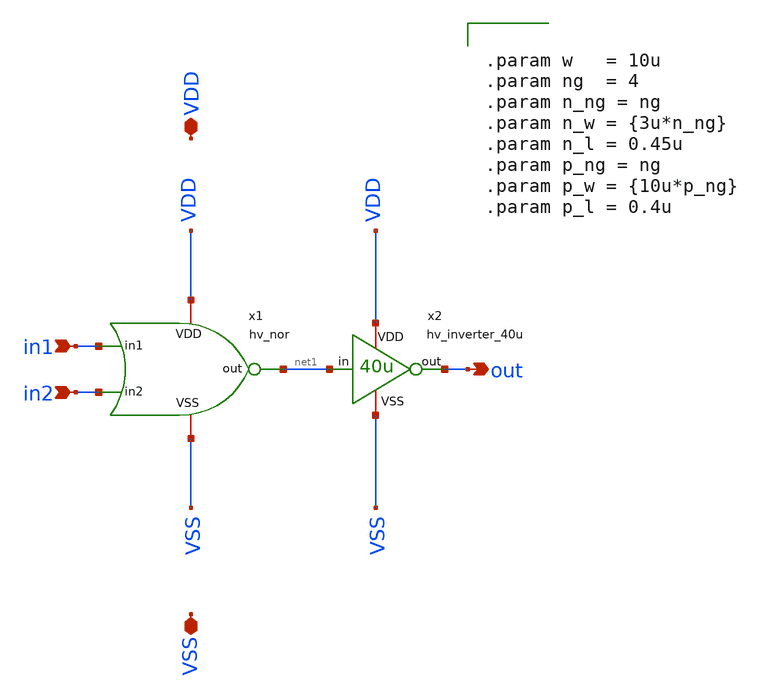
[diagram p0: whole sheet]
** sch_path: macros/heichips26_vcr/macros/switched_capacitor/schematic/xschem/hv_or.sch
**.subckt hv_or in1 VDD VSS in2 out
*.ipin in1
*.iopin VDD
*.iopin VSS
*.ipin in2
*.opin out
x1 VDD in1 net1 in2 VSS hv_nor
x2 VDD net1 out VSS hv_inverter_40u
**** begin user architecture code


.param w   = 10u
.param ng  = 4
.param n_ng = ng
.param n_w = {3u*n_ng}
.param n_l = 0.45u
.param p_ng = ng
.param p_w = {10u*p_ng}
.param p_l = 0.4u


**** end user architecture code
**.ends

* expanding   symbol:  hv_nor.sym # of pins=5
** sym_path: macros/heichips26_vcr/macros/switched_capacitor/schematic/xschem/hv_nor.sym
** sch_path: macros/heichips26_vcr/macros/switched_capacitor/schematic/xschem/hv_nor.sch
.subckt hv_nor VDD in1 out in2 VSS
*.ipin in1
*.iopin VDD
*.iopin VSS
*.opin out
*.ipin in2
**** begin user architecture code


.param w   = 10u
.param ng  = 4
.param n_ng = ng
.param n_w = {3u*n_ng}
.param n_l = 0.45u
.param p_ng = ng
.param p_w = {10u*p_ng}
.param p_l = 0.4u


**** end user architecture code
XM2 out in2 VSS VSS sg13_hv_nmos w={n_w} l={n_l} ng={ng} m=1 mm_ok=1
XM3 net1 in1 VDD VDD sg13_hv_pmos w={p_w} l={p_l} ng={ng} m=1 mm_ok=1
XM1 out in1 VSS VSS sg13_hv_nmos w={n_w} l={n_l} ng={ng} m=1 mm_ok=1
XM4 out in2 net1 VDD sg13_hv_pmos w={p_w} l={p_l} ng={ng} m=1 mm_ok=1
.ends


* expanding   symbol:  hv_inverter_40u.sym # of pins=4
** sym_path: macros/heichips26_vcr/macros/switched_capacitor/schematic/xschem/hv_inverter_40u.sym
** sch_path: macros/heichips26_vcr/macros/switched_capacitor/schematic/xschem/hv_inverter_40u.sch
.subckt hv_inverter_40u VDD in out VSS
*.ipin in
*.iopin VDD
*.iopin VSS
*.opin out
XM2 out in VSS VSS sg13_hv_nmos w={n_w} l={n_l} ng={ng} m=1 mm_ok=1
XM3 out in VDD VDD sg13_hv_pmos w={p_w} l={p_l} ng={ng} m=1 mm_ok=1
**** begin user architecture code


.param w   = 10u
.param ng  = 4
.param n_ng = ng
.param n_w = {3u*n_ng}
.param n_l = 0.45u
.param p_ng = ng
.param p_w = {10u*p_ng}
.param p_l = 0.4u


**** end user architecture code
.ends

.end
